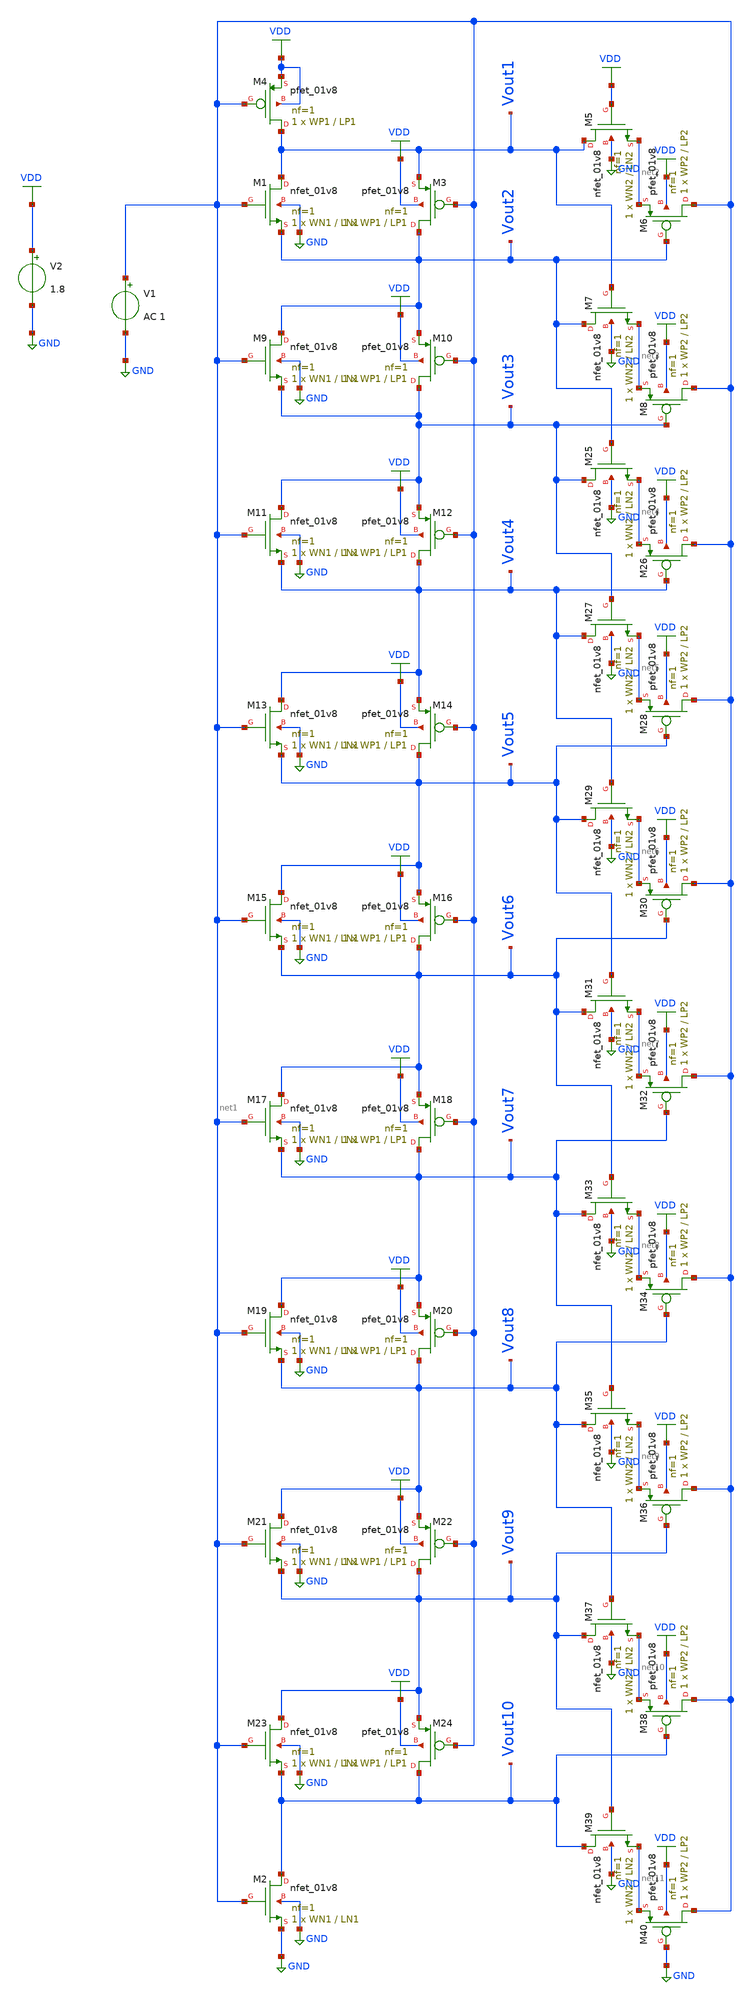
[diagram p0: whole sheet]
** sch_path: LIQAF circuit/10-Stage/10-stage LIQAF.sch
**.subckt 10-stage LIQAF
XM1 Vout1 net1 Vout2 GND sky130_fd_pr__nfet_01v8 L=LN1 W=WN1 nf=1 ad='int((nf+1)/2) * W/nf * 0.29' as='int((nf+2)/2) * W/nf * 0.29'
+ pd='2*int((nf+1)/2) * (W/nf + 0.29)' ps='2*int((nf+2)/2) * (W/nf + 0.29)' nrd='0.29 / W' nrs='0.29 / W'
+ sa=0 sb=0 sd=0 mult=1 m=1
V1 net1 GND AC 1
V2 VDD GND 1.8
XM2 Vout10 net1 GND GND sky130_fd_pr__nfet_01v8 L=LN1 W=WN1 nf=1 ad='int((nf+1)/2) * W/nf * 0.29' as='int((nf+2)/2) * W/nf * 0.29'
+ pd='2*int((nf+1)/2) * (W/nf + 0.29)' ps='2*int((nf+2)/2) * (W/nf + 0.29)' nrd='0.29 / W' nrs='0.29 / W'
+ sa=0 sb=0 sd=0 mult=1 m=1
XM3 Vout2 net1 Vout1 VDD sky130_fd_pr__pfet_01v8 L=LP1 W=WP1 nf=1 ad='int((nf+1)/2) * W/nf * 0.29' as='int((nf+2)/2) * W/nf * 0.29'
+ pd='2*int((nf+1)/2) * (W/nf + 0.29)' ps='2*int((nf+2)/2) * (W/nf + 0.29)' nrd='0.29 / W' nrs='0.29 / W'
+ sa=0 sb=0 sd=0 mult=1 m=1
XM4 Vout1 net1 VDD VDD sky130_fd_pr__pfet_01v8 L=LP1 W=WP1 nf=1 ad='int((nf+1)/2) * W/nf * 0.29' as='int((nf+2)/2) * W/nf * 0.29'
+ pd='2*int((nf+1)/2) * (W/nf + 0.29)' ps='2*int((nf+2)/2) * (W/nf + 0.29)' nrd='0.29 / W' nrs='0.29 / W'
+ sa=0 sb=0 sd=0 mult=1 m=1
XM5 Vout1 VDD net2 GND sky130_fd_pr__nfet_01v8 L=LN2 W=WN2 nf=1 ad='int((nf+1)/2) * W/nf * 0.29' as='int((nf+2)/2) * W/nf * 0.29'
+ pd='2*int((nf+1)/2) * (W/nf + 0.29)' ps='2*int((nf+2)/2) * (W/nf + 0.29)' nrd='0.29 / W' nrs='0.29 / W'
+ sa=0 sb=0 sd=0 mult=1 m=1
XM6 net1 Vout2 net2 VDD sky130_fd_pr__pfet_01v8 L=LP2 W=WP2 nf=1 ad='int((nf+1)/2) * W/nf * 0.29' as='int((nf+2)/2) * W/nf * 0.29'
+ pd='2*int((nf+1)/2) * (W/nf + 0.29)' ps='2*int((nf+2)/2) * (W/nf + 0.29)' nrd='0.29 / W' nrs='0.29 / W'
+ sa=0 sb=0 sd=0 mult=1 m=1
XM7 Vout2 Vout1 net3 GND sky130_fd_pr__nfet_01v8 L=LN2 W=WN2 nf=1 ad='int((nf+1)/2) * W/nf * 0.29' as='int((nf+2)/2) * W/nf * 0.29'
+ pd='2*int((nf+1)/2) * (W/nf + 0.29)' ps='2*int((nf+2)/2) * (W/nf + 0.29)' nrd='0.29 / W' nrs='0.29 / W'
+ sa=0 sb=0 sd=0 mult=1 m=1
XM8 net1 Vout3 net3 VDD sky130_fd_pr__pfet_01v8 L=LP2 W=WP2 nf=1 ad='int((nf+1)/2) * W/nf * 0.29' as='int((nf+2)/2) * W/nf * 0.29'
+ pd='2*int((nf+1)/2) * (W/nf + 0.29)' ps='2*int((nf+2)/2) * (W/nf + 0.29)' nrd='0.29 / W' nrs='0.29 / W'
+ sa=0 sb=0 sd=0 mult=1 m=1
XM9 Vout2 net1 Vout3 GND sky130_fd_pr__nfet_01v8 L=LN1 W=WN1 nf=1 ad='int((nf+1)/2) * W/nf * 0.29' as='int((nf+2)/2) * W/nf * 0.29'
+ pd='2*int((nf+1)/2) * (W/nf + 0.29)' ps='2*int((nf+2)/2) * (W/nf + 0.29)' nrd='0.29 / W' nrs='0.29 / W'
+ sa=0 sb=0 sd=0 mult=1 m=1
XM10 Vout3 net1 Vout2 VDD sky130_fd_pr__pfet_01v8 L=LP1 W=WP1 nf=1 ad='int((nf+1)/2) * W/nf * 0.29' as='int((nf+2)/2) * W/nf * 0.29'
+ pd='2*int((nf+1)/2) * (W/nf + 0.29)' ps='2*int((nf+2)/2) * (W/nf + 0.29)' nrd='0.29 / W' nrs='0.29 / W'
+ sa=0 sb=0 sd=0 mult=1 m=1
XM11 Vout3 net1 Vout4 GND sky130_fd_pr__nfet_01v8 L=LN1 W=WN1 nf=1 ad='int((nf+1)/2) * W/nf * 0.29' as='int((nf+2)/2) * W/nf * 0.29'
+ pd='2*int((nf+1)/2) * (W/nf + 0.29)' ps='2*int((nf+2)/2) * (W/nf + 0.29)' nrd='0.29 / W' nrs='0.29 / W'
+ sa=0 sb=0 sd=0 mult=1 m=1
XM12 Vout4 net1 Vout3 VDD sky130_fd_pr__pfet_01v8 L=LP1 W=WP1 nf=1 ad='int((nf+1)/2) * W/nf * 0.29' as='int((nf+2)/2) * W/nf * 0.29'
+ pd='2*int((nf+1)/2) * (W/nf + 0.29)' ps='2*int((nf+2)/2) * (W/nf + 0.29)' nrd='0.29 / W' nrs='0.29 / W'
+ sa=0 sb=0 sd=0 mult=1 m=1
XM13 Vout4 net1 Vout5 GND sky130_fd_pr__nfet_01v8 L=LN1 W=WN1 nf=1 ad='int((nf+1)/2) * W/nf * 0.29' as='int((nf+2)/2) * W/nf * 0.29'
+ pd='2*int((nf+1)/2) * (W/nf + 0.29)' ps='2*int((nf+2)/2) * (W/nf + 0.29)' nrd='0.29 / W' nrs='0.29 / W'
+ sa=0 sb=0 sd=0 mult=1 m=1
XM14 Vout5 net1 Vout4 VDD sky130_fd_pr__pfet_01v8 L=LP1 W=WP1 nf=1 ad='int((nf+1)/2) * W/nf * 0.29' as='int((nf+2)/2) * W/nf * 0.29'
+ pd='2*int((nf+1)/2) * (W/nf + 0.29)' ps='2*int((nf+2)/2) * (W/nf + 0.29)' nrd='0.29 / W' nrs='0.29 / W'
+ sa=0 sb=0 sd=0 mult=1 m=1
XM15 Vout5 net1 Vout6 GND sky130_fd_pr__nfet_01v8 L=LN1 W=WN1 nf=1 ad='int((nf+1)/2) * W/nf * 0.29' as='int((nf+2)/2) * W/nf * 0.29'
+ pd='2*int((nf+1)/2) * (W/nf + 0.29)' ps='2*int((nf+2)/2) * (W/nf + 0.29)' nrd='0.29 / W' nrs='0.29 / W'
+ sa=0 sb=0 sd=0 mult=1 m=1
XM16 Vout6 net1 Vout5 VDD sky130_fd_pr__pfet_01v8 L=LP1 W=WP1 nf=1 ad='int((nf+1)/2) * W/nf * 0.29' as='int((nf+2)/2) * W/nf * 0.29'
+ pd='2*int((nf+1)/2) * (W/nf + 0.29)' ps='2*int((nf+2)/2) * (W/nf + 0.29)' nrd='0.29 / W' nrs='0.29 / W'
+ sa=0 sb=0 sd=0 mult=1 m=1
XM17 Vout6 net1 Vout7 GND sky130_fd_pr__nfet_01v8 L=LN1 W=WN1 nf=1 ad='int((nf+1)/2) * W/nf * 0.29' as='int((nf+2)/2) * W/nf * 0.29'
+ pd='2*int((nf+1)/2) * (W/nf + 0.29)' ps='2*int((nf+2)/2) * (W/nf + 0.29)' nrd='0.29 / W' nrs='0.29 / W'
+ sa=0 sb=0 sd=0 mult=1 m=1
XM18 Vout7 net1 Vout6 VDD sky130_fd_pr__pfet_01v8 L=LP1 W=WP1 nf=1 ad='int((nf+1)/2) * W/nf * 0.29' as='int((nf+2)/2) * W/nf * 0.29'
+ pd='2*int((nf+1)/2) * (W/nf + 0.29)' ps='2*int((nf+2)/2) * (W/nf + 0.29)' nrd='0.29 / W' nrs='0.29 / W'
+ sa=0 sb=0 sd=0 mult=1 m=1
XM19 Vout7 net1 Vout8 GND sky130_fd_pr__nfet_01v8 L=LN1 W=WN1 nf=1 ad='int((nf+1)/2) * W/nf * 0.29' as='int((nf+2)/2) * W/nf * 0.29'
+ pd='2*int((nf+1)/2) * (W/nf + 0.29)' ps='2*int((nf+2)/2) * (W/nf + 0.29)' nrd='0.29 / W' nrs='0.29 / W'
+ sa=0 sb=0 sd=0 mult=1 m=1
XM20 Vout8 net1 Vout7 VDD sky130_fd_pr__pfet_01v8 L=LP1 W=WP1 nf=1 ad='int((nf+1)/2) * W/nf * 0.29' as='int((nf+2)/2) * W/nf * 0.29'
+ pd='2*int((nf+1)/2) * (W/nf + 0.29)' ps='2*int((nf+2)/2) * (W/nf + 0.29)' nrd='0.29 / W' nrs='0.29 / W'
+ sa=0 sb=0 sd=0 mult=1 m=1
XM21 Vout8 net1 Vout9 GND sky130_fd_pr__nfet_01v8 L=LN1 W=WN1 nf=1 ad='int((nf+1)/2) * W/nf * 0.29' as='int((nf+2)/2) * W/nf * 0.29'
+ pd='2*int((nf+1)/2) * (W/nf + 0.29)' ps='2*int((nf+2)/2) * (W/nf + 0.29)' nrd='0.29 / W' nrs='0.29 / W'
+ sa=0 sb=0 sd=0 mult=1 m=1
XM22 Vout9 net1 Vout8 VDD sky130_fd_pr__pfet_01v8 L=LP1 W=WP1 nf=1 ad='int((nf+1)/2) * W/nf * 0.29' as='int((nf+2)/2) * W/nf * 0.29'
+ pd='2*int((nf+1)/2) * (W/nf + 0.29)' ps='2*int((nf+2)/2) * (W/nf + 0.29)' nrd='0.29 / W' nrs='0.29 / W'
+ sa=0 sb=0 sd=0 mult=1 m=1
XM23 Vout9 net1 Vout10 GND sky130_fd_pr__nfet_01v8 L=LN1 W=WN1 nf=1 ad='int((nf+1)/2) * W/nf * 0.29'
+ as='int((nf+2)/2) * W/nf * 0.29' pd='2*int((nf+1)/2) * (W/nf + 0.29)' ps='2*int((nf+2)/2) * (W/nf + 0.29)'
+ nrd='0.29 / W' nrs='0.29 / W' sa=0 sb=0 sd=0 mult=1 m=1
XM24 Vout10 net1 Vout9 VDD sky130_fd_pr__pfet_01v8 L=LP1 W=WP1 nf=1 ad='int((nf+1)/2) * W/nf * 0.29'
+ as='int((nf+2)/2) * W/nf * 0.29' pd='2*int((nf+1)/2) * (W/nf + 0.29)' ps='2*int((nf+2)/2) * (W/nf + 0.29)'
+ nrd='0.29 / W' nrs='0.29 / W' sa=0 sb=0 sd=0 mult=1 m=1
XM25 Vout3 Vout2 net4 GND sky130_fd_pr__nfet_01v8 L=LN2 W=WN2 nf=1 ad='int((nf+1)/2) * W/nf * 0.29' as='int((nf+2)/2) * W/nf * 0.29'
+ pd='2*int((nf+1)/2) * (W/nf + 0.29)' ps='2*int((nf+2)/2) * (W/nf + 0.29)' nrd='0.29 / W' nrs='0.29 / W'
+ sa=0 sb=0 sd=0 mult=1 m=1
XM26 net1 Vout4 net4 VDD sky130_fd_pr__pfet_01v8 L=LP2 W=WP2 nf=1 ad='int((nf+1)/2) * W/nf * 0.29' as='int((nf+2)/2) * W/nf * 0.29'
+ pd='2*int((nf+1)/2) * (W/nf + 0.29)' ps='2*int((nf+2)/2) * (W/nf + 0.29)' nrd='0.29 / W' nrs='0.29 / W'
+ sa=0 sb=0 sd=0 mult=1 m=1
XM27 Vout4 Vout3 net5 GND sky130_fd_pr__nfet_01v8 L=LN2 W=WN2 nf=1 ad='int((nf+1)/2) * W/nf * 0.29' as='int((nf+2)/2) * W/nf * 0.29'
+ pd='2*int((nf+1)/2) * (W/nf + 0.29)' ps='2*int((nf+2)/2) * (W/nf + 0.29)' nrd='0.29 / W' nrs='0.29 / W'
+ sa=0 sb=0 sd=0 mult=1 m=1
XM28 net1 Vout5 net5 VDD sky130_fd_pr__pfet_01v8 L=LP2 W=WP2 nf=1 ad='int((nf+1)/2) * W/nf * 0.29' as='int((nf+2)/2) * W/nf * 0.29'
+ pd='2*int((nf+1)/2) * (W/nf + 0.29)' ps='2*int((nf+2)/2) * (W/nf + 0.29)' nrd='0.29 / W' nrs='0.29 / W'
+ sa=0 sb=0 sd=0 mult=1 m=1
XM29 Vout5 Vout4 net6 GND sky130_fd_pr__nfet_01v8 L=LN2 W=WN2 nf=1 ad='int((nf+1)/2) * W/nf * 0.29' as='int((nf+2)/2) * W/nf * 0.29'
+ pd='2*int((nf+1)/2) * (W/nf + 0.29)' ps='2*int((nf+2)/2) * (W/nf + 0.29)' nrd='0.29 / W' nrs='0.29 / W'
+ sa=0 sb=0 sd=0 mult=1 m=1
XM30 net1 Vout6 net6 VDD sky130_fd_pr__pfet_01v8 L=LP2 W=WP2 nf=1 ad='int((nf+1)/2) * W/nf * 0.29' as='int((nf+2)/2) * W/nf * 0.29'
+ pd='2*int((nf+1)/2) * (W/nf + 0.29)' ps='2*int((nf+2)/2) * (W/nf + 0.29)' nrd='0.29 / W' nrs='0.29 / W'
+ sa=0 sb=0 sd=0 mult=1 m=1
XM31 Vout6 Vout5 net7 GND sky130_fd_pr__nfet_01v8 L=LN2 W=WN2 nf=1 ad='int((nf+1)/2) * W/nf * 0.29' as='int((nf+2)/2) * W/nf * 0.29'
+ pd='2*int((nf+1)/2) * (W/nf + 0.29)' ps='2*int((nf+2)/2) * (W/nf + 0.29)' nrd='0.29 / W' nrs='0.29 / W'
+ sa=0 sb=0 sd=0 mult=1 m=1
XM32 net1 Vout7 net7 VDD sky130_fd_pr__pfet_01v8 L=LP2 W=WP2 nf=1 ad='int((nf+1)/2) * W/nf * 0.29' as='int((nf+2)/2) * W/nf * 0.29'
+ pd='2*int((nf+1)/2) * (W/nf + 0.29)' ps='2*int((nf+2)/2) * (W/nf + 0.29)' nrd='0.29 / W' nrs='0.29 / W'
+ sa=0 sb=0 sd=0 mult=1 m=1
XM33 Vout7 Vout6 net8 GND sky130_fd_pr__nfet_01v8 L=LN2 W=WN2 nf=1 ad='int((nf+1)/2) * W/nf * 0.29' as='int((nf+2)/2) * W/nf * 0.29'
+ pd='2*int((nf+1)/2) * (W/nf + 0.29)' ps='2*int((nf+2)/2) * (W/nf + 0.29)' nrd='0.29 / W' nrs='0.29 / W'
+ sa=0 sb=0 sd=0 mult=1 m=1
XM34 net1 Vout8 net8 VDD sky130_fd_pr__pfet_01v8 L=LP2 W=WP2 nf=1 ad='int((nf+1)/2) * W/nf * 0.29' as='int((nf+2)/2) * W/nf * 0.29'
+ pd='2*int((nf+1)/2) * (W/nf + 0.29)' ps='2*int((nf+2)/2) * (W/nf + 0.29)' nrd='0.29 / W' nrs='0.29 / W'
+ sa=0 sb=0 sd=0 mult=1 m=1
XM35 Vout8 Vout7 net9 GND sky130_fd_pr__nfet_01v8 L=LN2 W=WN2 nf=1 ad='int((nf+1)/2) * W/nf * 0.29' as='int((nf+2)/2) * W/nf * 0.29'
+ pd='2*int((nf+1)/2) * (W/nf + 0.29)' ps='2*int((nf+2)/2) * (W/nf + 0.29)' nrd='0.29 / W' nrs='0.29 / W'
+ sa=0 sb=0 sd=0 mult=1 m=1
XM36 net1 Vout9 net9 VDD sky130_fd_pr__pfet_01v8 L=LP2 W=WP2 nf=1 ad='int((nf+1)/2) * W/nf * 0.29' as='int((nf+2)/2) * W/nf * 0.29'
+ pd='2*int((nf+1)/2) * (W/nf + 0.29)' ps='2*int((nf+2)/2) * (W/nf + 0.29)' nrd='0.29 / W' nrs='0.29 / W'
+ sa=0 sb=0 sd=0 mult=1 m=1
XM37 Vout9 Vout8 net10 GND sky130_fd_pr__nfet_01v8 L=LN2 W=WN2 nf=1 ad='int((nf+1)/2) * W/nf * 0.29'
+ as='int((nf+2)/2) * W/nf * 0.29' pd='2*int((nf+1)/2) * (W/nf + 0.29)' ps='2*int((nf+2)/2) * (W/nf + 0.29)'
+ nrd='0.29 / W' nrs='0.29 / W' sa=0 sb=0 sd=0 mult=1 m=1
XM38 net1 Vout10 net10 VDD sky130_fd_pr__pfet_01v8 L=LP2 W=WP2 nf=1 ad='int((nf+1)/2) * W/nf * 0.29'
+ as='int((nf+2)/2) * W/nf * 0.29' pd='2*int((nf+1)/2) * (W/nf + 0.29)' ps='2*int((nf+2)/2) * (W/nf + 0.29)'
+ nrd='0.29 / W' nrs='0.29 / W' sa=0 sb=0 sd=0 mult=1 m=1
XM39 Vout10 Vout9 net11 GND sky130_fd_pr__nfet_01v8 L=LN2 W=WN2 nf=1 ad='int((nf+1)/2) * W/nf * 0.29'
+ as='int((nf+2)/2) * W/nf * 0.29' pd='2*int((nf+1)/2) * (W/nf + 0.29)' ps='2*int((nf+2)/2) * (W/nf + 0.29)'
+ nrd='0.29 / W' nrs='0.29 / W' sa=0 sb=0 sd=0 mult=1 m=1
XM40 net1 GND net11 VDD sky130_fd_pr__pfet_01v8 L=LP2 W=WP2 nf=1 ad='int((nf+1)/2) * W/nf * 0.29' as='int((nf+2)/2) * W/nf * 0.29'
+ pd='2*int((nf+1)/2) * (W/nf + 0.29)' ps='2*int((nf+2)/2) * (W/nf + 0.29)' nrd='0.29 / W' nrs='0.29 / W'
+ sa=0 sb=0 sd=0 mult=1 m=1
**** begin user architecture code
 ** manual skywater pdks install (with patches applied)
* .lib $::SKYWATER_MODELS/models/sky130.lib.spice tt

** opencircuitdesign pdks install
.lib $::SKYWATER_MODELS/sky130.lib.spice tt

.param mc_mm_switch=0
.param mc_pr_switch=0
.param LP1=0.15


.dc V1 0 1.8 0.01
.control
run
plot v(Vout1) v(Vout2) v(Vout3) v(Vout4) v(Vout5) v(Vout6) v(Vout7) v(Vout8) v(Vout9) v(Vout10)
.endc
.save all



.param LP1=0.15
.param WP1=25
.param LN1=0.15
.param WN1=12.5

.param LP2=0.15
.param WP2=5
.param LN2=0.15
.param WN2=25


**** end user architecture code
**.ends
.GLOBAL GND
.GLOBAL VDD
.end
